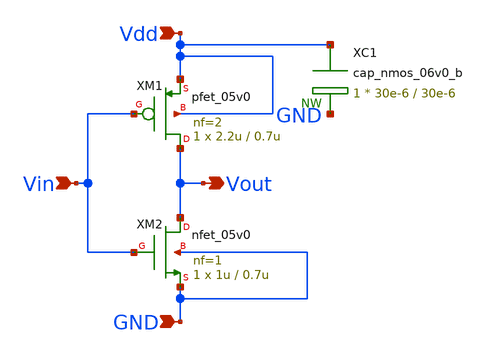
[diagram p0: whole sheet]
** sch_path: MG_decoder/MG_not_gate.sch
**.subckt MG_not_gate Vdd GND Vin Vout
*.ipin Vdd
*.ipin GND
*.ipin Vin
*.opin Vout
XM1 Vout Vin Vdd Vdd pfet_05v0 L=0.7u W=2.2u nf=2 ad='int((nf+1)/2) * W/nf * 0.18u' as='int((nf+2)/2) * W/nf * 0.18u'
+ pd='2*int((nf+1)/2) * (W/nf + 0.18u)' ps='2*int((nf+2)/2) * (W/nf + 0.18u)' nrd='0.18u / W' nrs='0.18u / W'
+ sa=0 sb=0 sd=0 m=1
XM2 Vout Vin GND GND nfet_05v0 L=0.7u W=1u nf=1 ad='int((nf+1)/2) * W/nf * 0.18u' as='int((nf+2)/2) * W/nf * 0.18u'
+ pd='2*int((nf+1)/2) * (W/nf + 0.18u)' ps='2*int((nf+2)/2) * (W/nf + 0.18u)' nrd='0.18u / W' nrs='0.18u / W'
+ sa=0 sb=0 sd=0 m=1
XC1 Vdd GND cap_nmos_06v0_b c_width=30e-6 c_length=30e-6 m=1
**.ends
.end
